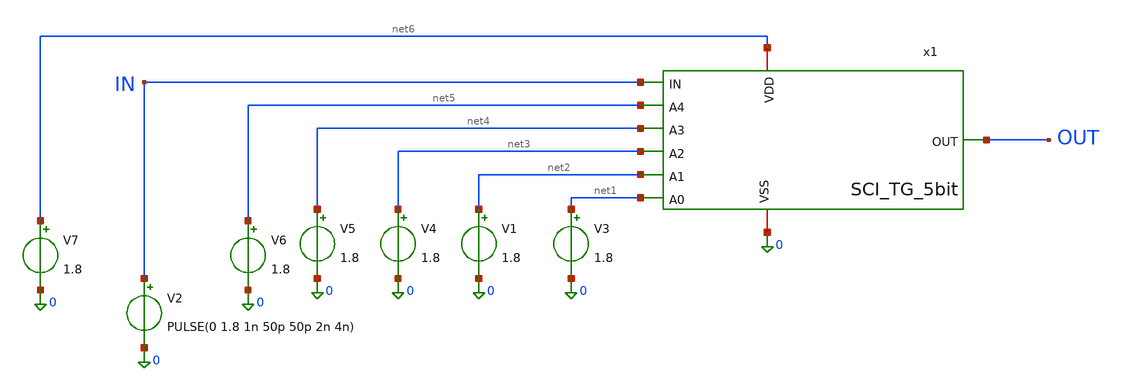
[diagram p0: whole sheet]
** sch_path: xschem/schematic/SCI_DCDL/TG_SCI/TB_TG5bit.sch
**.subckt TB_TG5bit
V2 IN 0 PULSE(0 1.8 1n 50p 50p 2n 4n)
V3 net1 0 1.8
V1 net2 0 1.8
V4 net3 0 1.8
V5 net4 0 1.8
V6 net5 0 1.8
V7 net6 0 1.8
x1 net6 IN OUT 0 net3 net5 net4 net2 net1 SCI_TG_5bit
**** begin user architecture code


.option rshunt=1e12
.tran 1p 25n 0 1p

.control

* Save signals for measurement
save v(IN) v(OUT)

* Output file
echo code t_rise_ps t_fall_ps t_pd_ps >
+ /home/xiaohi/Projects/sky130_dcdl/results/csv/sci_tg_5bit.dat

* Sweep 32 control codes
foreach b4 0 1
 foreach b3 0 1
  foreach b2 0 1
   foreach b1 0 1
    foreach b0 0 1

     * Calculate control voltages
     let v0 = 1.8 * $b0
     let v1 = 1.8 * $b1
     let v2 = 1.8 * $b2
     let v3 = 1.8 * $b3
     let v4 = 1.8 * $b4

     * Update voltage sources
     alter V3 dc = $&v0
     alter V1 dc = $&v1
     alter V4 dc = $&v2
     alter V5 dc = $&v3
     alter V6 dc = $&v4

     * Run transient
     run

     * Propagation delay: two inverters
     meas tran t_rise TRIG v(IN) VAL=0.9 RISE=2 TARG v(OUT) VAL=0.9 RISE=2

     meas tran t_fall TRIG v(IN) VAL=0.9 FALL=2 TARG v(OUT) VAL=0.9 FALL=2

     * Calculate delay in ps
     let code = 16*$b4 + 8*$b3 + 4*$b2 + 2*$b1 + $b0

     let rise_ps = t_rise * 1e12
     let fall_ps = t_fall * 1e12
     let pd_ps = (rise_ps + fall_ps)/2

     * Write results
     echo $&code $&rise_ps $&fall_ps $&pd_ps >>
+ /home/xiaohi/Projects/sky130_dcdl/results/csv/sci_tg_5bit.dat

    end
   end
  end
 end
end

echo SCI TG 5-bit sweep completed
.endc



** opencircuitdesign pdks install
.lib $::SKYWATER_MODELS/sky130.lib.spice tt

**** end user architecture code
**.ends

* expanding   symbol:  SCI_TG_5bit.sym # of pins=9
** sym_path: xschem/schematic/SCI_DCDL/TG_SCI/SCI_TG_5bit.sym
** sch_path: xschem/schematic/SCI_DCDL/TG_SCI/SCI_TG_5bit.sch
.subckt SCI_TG_5bit VDD IN OUT VSS A2 A4 A3 A1 A0
*.ipin IN
*.opin OUT
*.iopin VDD
*.iopin VSS
*.ipin A0
*.ipin A1
*.ipin A2
*.ipin A3
*.ipin A4
XM1 net1 IN VSS VSS sky130_fd_pr__nfet_01v8 L=0.15 W=1 nf=1 ad='int((1 + 1)/2) * 1 / 1 * 0.29' as='int((1 + 2)/2) * 1 / 1 * 0.29'
+ pd='2*int((1 + 1)/2) * (1 / 1 + 0.29)' ps='2*int((1 + 2)/2) * (1 / 1 + 0.29)' nrd='0.29 / 1 ' nrs='0.29 / 1 '
+ sa=0 sb=0 sd=0 mult=1 m=1
XM3 OUT net1 VSS VSS sky130_fd_pr__nfet_01v8 L=0.15 W=1 nf=1 ad='int((1 + 1)/2) * 1 / 1 * 0.29' as='int((1 + 2)/2) * 1 / 1 * 0.29'
+ pd='2*int((1 + 1)/2) * (1 / 1 + 0.29)' ps='2*int((1 + 2)/2) * (1 / 1 + 0.29)' nrd='0.29 / 1 ' nrs='0.29 / 1 '
+ sa=0 sb=0 sd=0 mult=1 m=1
XM5 net1 IN VDD VDD sky130_fd_pr__pfet_01v8 L=0.15 W=2.5 nf=1 ad='int((1 + 1)/2) * 2.5 / 1 * 0.29' as='int((1 + 2)/2) * 2.5 / 1 * 0.29'
+ pd='2*int((1 + 1)/2) * (2.5 / 1 + 0.29)' ps='2*int((1 + 2)/2) * (2.5 / 1 + 0.29)' nrd='0.29 / 2.5 ' nrs='0.29 / 2.5 '
+ sa=0 sb=0 sd=0 mult=1 m=1
XM2 OUT net1 VDD VDD sky130_fd_pr__pfet_01v8 L=0.15 W=2.5 nf=1 ad='int((1 + 1)/2) * 2.5 / 1 * 0.29' as='int((1 + 2)/2) * 2.5 / 1 * 0.29'
+ pd='2*int((1 + 1)/2) * (2.5 / 1 + 0.29)' ps='2*int((1 + 2)/2) * (2.5 / 1 + 0.29)' nrd='0.29 / 2.5 ' nrs='0.29 / 2.5 '
+ sa=0 sb=0 sd=0 mult=1 m=1
XM4 net1 A0 net2 VSS sky130_fd_pr__nfet_01v8 L=0.15 W=0.5 nf=1 ad='int((1 + 1)/2) * 0.5 / 1 * 0.29' as='int((1 + 2)/2) * 0.5 / 1 * 0.29'
+ pd='2*int((1 + 1)/2) * (0.5 / 1 + 0.29)' ps='2*int((1 + 2)/2) * (0.5 / 1 + 0.29)' nrd='0.29 / 0.5 ' nrs='0.29 / 0.5 '
+ sa=0 sb=0 sd=0 mult=1 m=1
XM10 net1 net3 net2 VDD sky130_fd_pr__pfet_01v8 L=0.15 W=0.5 nf=1 ad='int((1 + 1)/2) * 0.5 / 1 * 0.29'
+ as='int((1 + 2)/2) * 0.5 / 1 * 0.29' pd='2*int((1 + 1)/2) * (0.5 / 1 + 0.29)' ps='2*int((1 + 2)/2) * (0.5 / 1 + 0.29)'
+ nrd='0.29 / 0.5 ' nrs='0.29 / 0.5 ' sa=0 sb=0 sd=0 mult=1 m=1
x1 VDD A0 net3 VSS inverter
XM6 net1 A1 net4 VSS sky130_fd_pr__nfet_01v8 L=0.15 W=1 nf=1 ad='int((1 + 1)/2) * 1 / 1 * 0.29' as='int((1 + 2)/2) * 1 / 1 * 0.29'
+ pd='2*int((1 + 1)/2) * (1 / 1 + 0.29)' ps='2*int((1 + 2)/2) * (1 / 1 + 0.29)' nrd='0.29 / 1 ' nrs='0.29 / 1 '
+ sa=0 sb=0 sd=0 mult=1 m=1
XM7 net1 net5 net4 VDD sky130_fd_pr__pfet_01v8 L=0.15 W=1 nf=1 ad='int((1 + 1)/2) * 1 / 1 * 0.29' as='int((1 + 2)/2) * 1 / 1 * 0.29'
+ pd='2*int((1 + 1)/2) * (1 / 1 + 0.29)' ps='2*int((1 + 2)/2) * (1 / 1 + 0.29)' nrd='0.29 / 1 ' nrs='0.29 / 1 '
+ sa=0 sb=0 sd=0 mult=1 m=1
x2 VDD A1 net5 VSS inverter
XM8 net1 A2 net6 VSS sky130_fd_pr__nfet_01v8 L=0.15 W=2 nf=1 ad='int((1 + 1)/2) * 2 / 1 * 0.29' as='int((1 + 2)/2) * 2 / 1 * 0.29'
+ pd='2*int((1 + 1)/2) * (2 / 1 + 0.29)' ps='2*int((1 + 2)/2) * (2 / 1 + 0.29)' nrd='0.29 / 2 ' nrs='0.29 / 2 '
+ sa=0 sb=0 sd=0 mult=1 m=1
XM9 net1 net7 net6 VDD sky130_fd_pr__pfet_01v8 L=0.15 W=2 nf=1 ad='int((1 + 1)/2) * 2 / 1 * 0.29' as='int((1 + 2)/2) * 2 / 1 * 0.29'
+ pd='2*int((1 + 1)/2) * (2 / 1 + 0.29)' ps='2*int((1 + 2)/2) * (2 / 1 + 0.29)' nrd='0.29 / 2 ' nrs='0.29 / 2 '
+ sa=0 sb=0 sd=0 mult=1 m=1
x3 VDD A2 net7 VSS inverter
XM11 net1 A3 net8 VSS sky130_fd_pr__nfet_01v8 L=0.15 W=4 nf=1 ad='int((1 + 1)/2) * 4 / 1 * 0.29' as='int((1 + 2)/2) * 4 / 1 * 0.29'
+ pd='2*int((1 + 1)/2) * (4 / 1 + 0.29)' ps='2*int((1 + 2)/2) * (4 / 1 + 0.29)' nrd='0.29 / 4 ' nrs='0.29 / 4 '
+ sa=0 sb=0 sd=0 mult=1 m=1
XM12 net1 net9 net8 VDD sky130_fd_pr__pfet_01v8 L=0.15 W=4 nf=1 ad='int((1 + 1)/2) * 4 / 1 * 0.29' as='int((1 + 2)/2) * 4 / 1 * 0.29'
+ pd='2*int((1 + 1)/2) * (4 / 1 + 0.29)' ps='2*int((1 + 2)/2) * (4 / 1 + 0.29)' nrd='0.29 / 4 ' nrs='0.29 / 4 '
+ sa=0 sb=0 sd=0 mult=1 m=1
x4 VDD A3 net9 VSS inverter
XM13 net1 A4 net10 VSS sky130_fd_pr__nfet_01v8 L=0.15 W=8 nf=1 ad='int((1 + 1)/2) * 8 / 1 * 0.29' as='int((1 + 2)/2) * 8 / 1 * 0.29'
+ pd='2*int((1 + 1)/2) * (8 / 1 + 0.29)' ps='2*int((1 + 2)/2) * (8 / 1 + 0.29)' nrd='0.29 / 8 ' nrs='0.29 / 8 '
+ sa=0 sb=0 sd=0 mult=1 m=1
XM14 net1 net11 net10 VDD sky130_fd_pr__pfet_01v8 L=0.15 W=8 nf=1 ad='int((1 + 1)/2) * 8 / 1 * 0.29'
+ as='int((1 + 2)/2) * 8 / 1 * 0.29' pd='2*int((1 + 1)/2) * (8 / 1 + 0.29)' ps='2*int((1 + 2)/2) * (8 / 1 + 0.29)'
+ nrd='0.29 / 8 ' nrs='0.29 / 8 ' sa=0 sb=0 sd=0 mult=1 m=1
x5 VDD A4 net11 VSS inverter
.ends


* expanding   symbol:  inverter.sym # of pins=4
** sym_path: xschem/schematic/SCI_DCDL/TG_SCI/inverter.sym
** sch_path: xschem/schematic/SCI_DCDL/TG_SCI/inverter.sch
.subckt inverter VDD IN OUT VSS
*.ipin IN
*.opin OUT
*.iopin VDD
*.iopin VSS
XM1 OUT IN VSS VSS sky130_fd_pr__nfet_01v8 L=0.15 W=1 nf=1 ad='int((1 + 1)/2) * 1 / 1 * 0.29' as='int((1 + 2)/2) * 1 / 1 * 0.29'
+ pd='2*int((1 + 1)/2) * (1 / 1 + 0.29)' ps='2*int((1 + 2)/2) * (1 / 1 + 0.29)' nrd='0.29 / 1 ' nrs='0.29 / 1 '
+ sa=0 sb=0 sd=0 mult=1 m=1
XM2 OUT IN VDD VDD sky130_fd_pr__pfet_01v8 L=0.15 W=1 nf=1 ad='int((1 + 1)/2) * 1 / 1 * 0.29' as='int((1 + 2)/2) * 1 / 1 * 0.29'
+ pd='2*int((1 + 1)/2) * (1 / 1 + 0.29)' ps='2*int((1 + 2)/2) * (1 / 1 + 0.29)' nrd='0.29 / 1 ' nrs='0.29 / 1 '
+ sa=0 sb=0 sd=0 mult=1 m=1
.ends

.end
